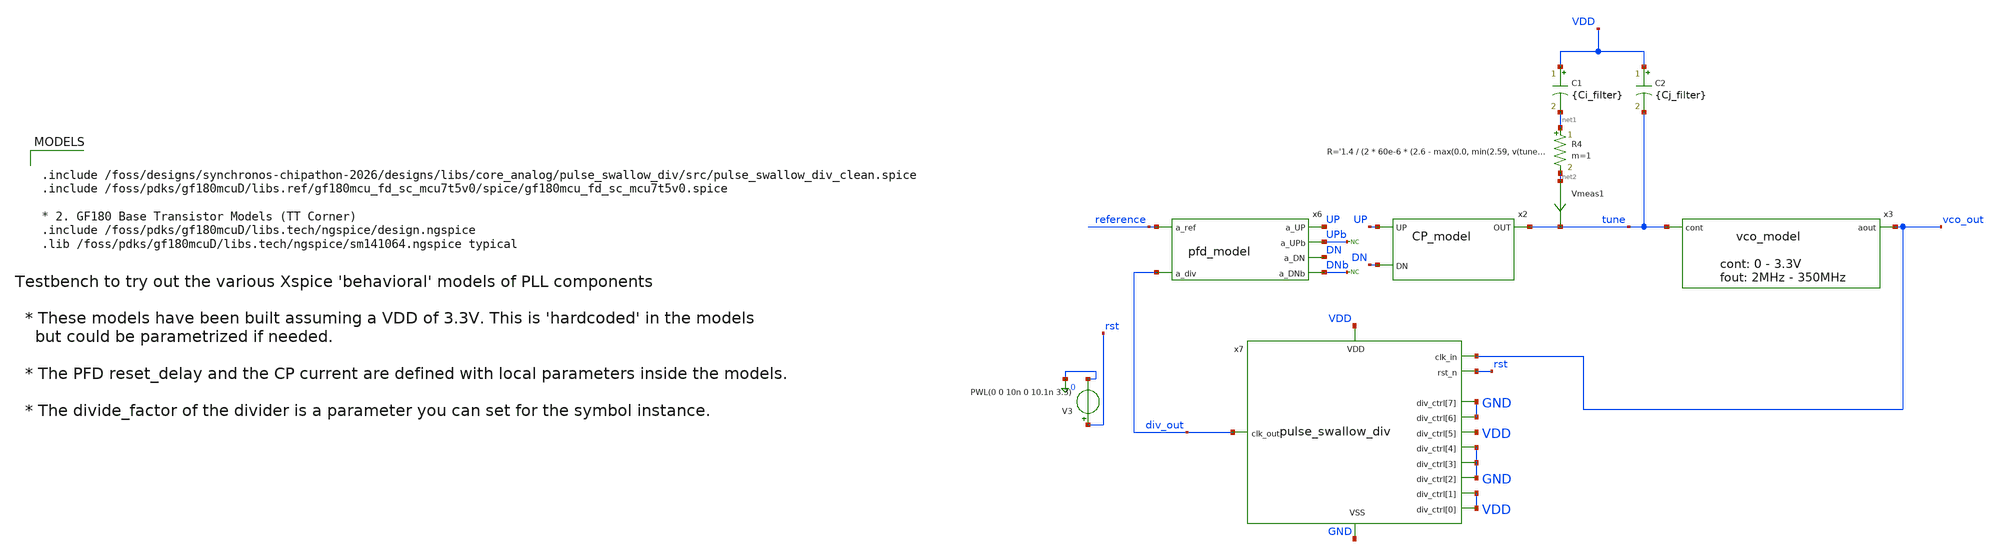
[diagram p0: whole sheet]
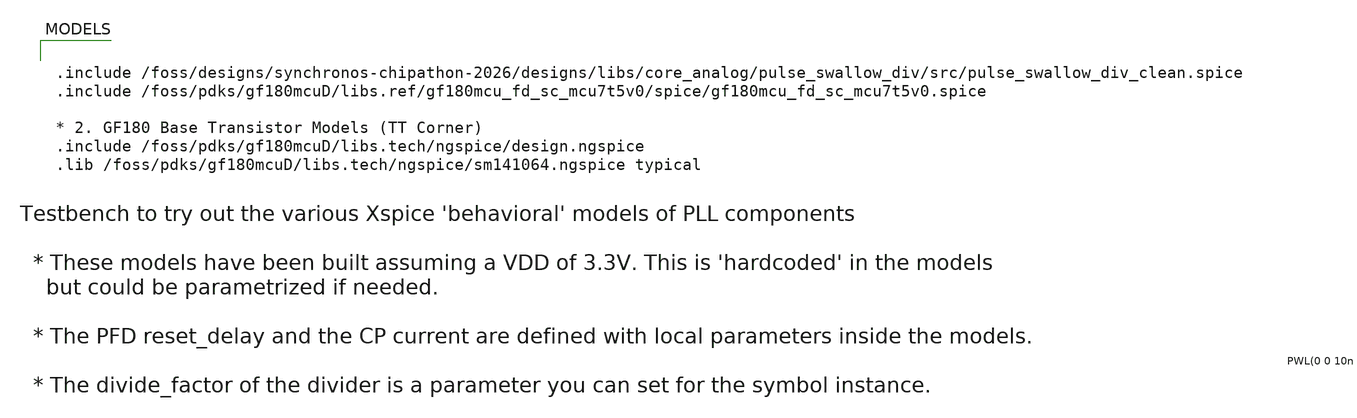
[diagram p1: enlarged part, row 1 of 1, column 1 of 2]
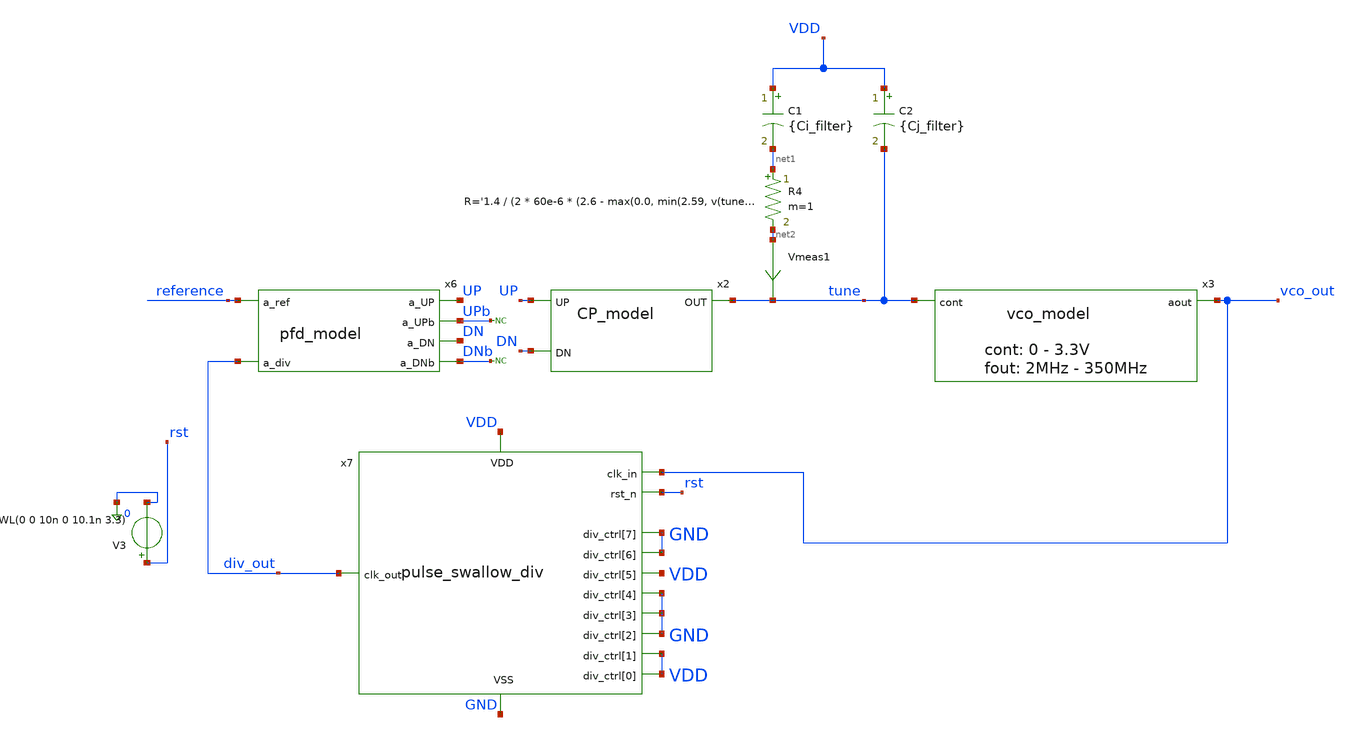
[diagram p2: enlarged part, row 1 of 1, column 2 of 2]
** sch_path: designs/libs/tb_pll/tb_PLL_div_model.sch
**.subckt tb_PLL_div_model
C1 VDD net1 {Ci_filter} m=1
R4 net1 net2 R='1.4 / (2 * 60e-6 * (2.6 - max(0.0, min(2.59, v(tune)))))' m=1
* noconn DNb
* noconn UPb
C2 VDD tune {Cj_filter} m=1
x2 tune UP DN CP_model
x3 vco_out tune vco_model
Vmeas1 net2 tune 0
.save i(vmeas1)
x7 VDD GND vco_out div_out VDD VDD GND GND GND VDD GND GND rst pulse_swallow_div
x6 reference UP UPb DN div_out DNb pfd_model
V3 rst 0 PWL(0 0 10n 0 10.1n 3.3)
**** begin user architecture code

.include /foss/designs/synchronos-chipathon-2026/designs/libs/core_analog/pulse_swallow_div/src/pulse_swallow_div_clean.spice
.include /foss/pdks/gf180mcuD/libs.ref/gf180mcu_fd_sc_mcu7t5v0/spice/gf180mcu_fd_sc_mcu7t5v0.spice

* 2. GF180 Base Transistor Models (TT Corner)
.include /foss/pdks/gf180mcuD/libs.tech/ngspice/design.ngspice
.lib /foss/pdks/gf180mcuD/libs.tech/ngspice/sm141064.ngspice typical



.options method=gear
VDD VDD 0 3.3
* control is for tests when opening the loop
* see the Vcontrol voltage source
.ic v(tune)=3.2
* reference frequency
.param f_ref = 10MEG
* divider
.param R_div=2
.param N_div=70
* loop filter parameters
.param Ci_filter = 10p
.param Cj_filter = 1p
.param td_ref='1/f_ref' tp_ref='td_ref/2'
Vref reference gnd pulse(0 3.3 0 10p 10p tp_ref td_ref)

.control
set wr_singlescale
set wr_vecnames

*save all
save v(vco_out) v(reference) v(up) v(dn) v(tune) v(pre_div) v(div_out)
TRAN 10n 200u
remzerovec

write tb_PLL_div_model.raw
wrdata /foss/designs/synchronos-chipathon-2026/designs/libs/scripts/sim_data/tb_PLL_div_model.txt
+ tran.all
.endc


**** end user architecture code
**.ends

* expanding   symbol:  libs/model_pll/CP_model.sym # of pins=3
** sym_path: designs/libs/model_pll/CP_model.sym
** sch_path: designs/libs/model_pll/CP_model.sch
.subckt CP_model OUT UP DN
*.ipin UP
*.ipin DN
*.opin OUT
**** begin user architecture code


* Bulletproof Charge Pump: Continuous Triode-Region Soft-Clipping
.param param_k = 60e-6

* UP (Sinks to Ground): Smoothly rolls off current as Vctrl drops from 0.1V to 0V
B_Iup OUT 0 I='V(UP) > 1.65 ? (param_k * ((2.6 - max(0.2, min(2.6, V(OUT))))^2 + 0.001)) * max(0, min(1, V(OUT)/0.1)) : 0'

* DN (Sources from VDD): Smoothly rolls off current as Vctrl rises from 3.2V to 3.3V
B_Idn OUT 0 I='V(DN) > 1.65 ? -(param_k * ((2.6 - max(0.2, min(2.6, V(OUT))))^2 + 0.001)) * max(0, min(1, (3.3 - V(OUT))/0.1)) : 0'


**** end user architecture code
* noconn UP
* noconn DN
* noconn OUT
.ends


* expanding   symbol:  libs/model_pll/vco_model.sym # of pins=2
** sym_path: designs/libs/model_pll/vco_model.sym
** sch_path: designs/libs/model_pll/vco_model.sch
.subckt vco_model aout cont
*.ipin cont
*.opin aout
**** begin user architecture code


***** XSPICE analog sine VCO ***************

.param vdd=3.3
.param vthp=0.7
.param vdsat=0.2
.param upper_limit=vdd-vthp-vdsat
.param lower_limit=0.2
asine cont aout analog_sin_osc
.model analog_sin_osc sine(  cntl_array = [ 0.0  3.3 ]   freq_array = [ 400MEG 10k  ]  out_high =
+ 3.3 out_low = 0.0 )


**** end user architecture code
* noconn aout
* noconn cont
.ends


* expanding   symbol:  libs/model_pll/pfd_model.sym # of pins=6
** sym_path: designs/libs/model_pll/pfd_model.sym
** sch_path: designs/libs/model_pll/pfd_model.sch
.subckt pfd_model a_ref a_UP a_UPb a_DN a_div a_DNb
*.ipin a_ref
*.ipin a_div
*.opin a_UP
*.opin a_UPb
*.opin a_DN
*.opin a_DNb
* noconn a_ref
* noconn a_div
* noconn a_UP
* noconn a_UPb
* noconn a_DN
* noconn a_DNb
**** begin user architecture code


* PFD Model using digital Xspice components

* pfd_delay local parameter sets the duration of the overlap (dead-band elimination)
* Reduced from 10ns to 200ps to prevent massive Vctrl ripple
*.param pfd_delay = 200p
.param pfd_delay = 1.5n

** Digital 1 and 0 to drive Flip-Flops
aone 0 d_d1 d_inv
azero d_d1 d_d0 d_inv
.model d_inv d_inverter()

** Flip Flops
ad1 d_d1 d_R d_d0 d_rset d_U d_U_ flop1
ad2 d_d1 d_V d_d0 d_rset d_D d_D_ flop1
.model flop1 d_dff(clk_delay = 1.0e-10 set_delay = 1.0e-10  reset_delay = {pfd_delay} ic = 2 rise_delay
+ = 1.0e-10  fall_delay = 1e-10)

* AND Gate
aa1 [d_U d_D] d_rset and1
.model and1 d_and(rise_delay = 1e-10 fall_delay = 1e-10   input_load = 0.5e-12)

* WINDOW FIX: Widened thresholds to catch fast analog edges safely
aADC [ a_ref a_div ] [ d_R d_V ] adc_buff
.model adc_buff adc_bridge(in_low = 1.2 in_high = 2.1 rise_delay = 10p fall_delay = 10p)

* DAC FIX: Explicitly defined analog rise/fall times to prevent solver crashes
aDAC [ d_U d_U_ d_D d_D_ d_rset d_R d_V d_d1 d_d0 ] [ a_UP a_UPb a_DN a_DNb a_rset a_R a_V a_d1
+ a_d0] dac_buff
.model dac_buff dac_bridge(out_low = 0 out_high = 3.3 t_rise = 500p t_fall = 500p)


**** end user architecture code
.ends

.end
